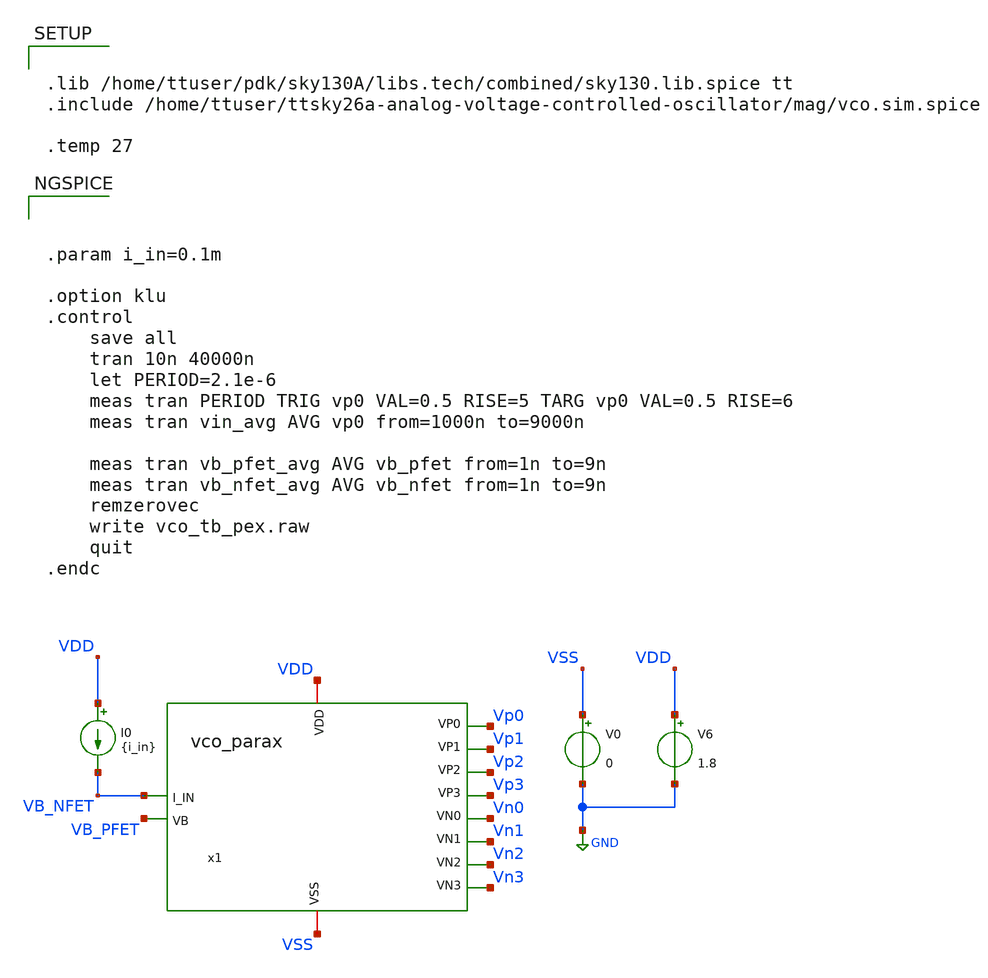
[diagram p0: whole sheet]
** sch_path: xschem/vco_tb_pex.sch
**.subckt vco_tb_pex
V0 VSS GND 0
V6 VDD GND 1.8
I0 VDD VB_NFET {i_in}
x1 VDD VSS VB_NFET Vp0 Vp1 Vp2 Vp3 Vn0 Vn1 Vn2 Vn3 VB_PFET vco_parax
**** begin user architecture code



.param i_in=0.1m

.option klu
.control
	save all
	tran 10n 40000n
	let PERIOD=2.1e-6
	meas tran PERIOD TRIG vp0 VAL=0.5 RISE=5 TARG vp0 VAL=0.5 RISE=6
	meas tran vin_avg AVG vp0 from=1000n to=9000n

	meas tran vb_pfet_avg AVG vb_pfet from=1n to=9n
	meas tran vb_nfet_avg AVG vb_nfet from=1n to=9n
	remzerovec
	write vco_tb_pex.raw
	quit
.endc




.lib /home/ttuser/pdk/sky130A/libs.tech/combined/sky130.lib.spice tt
.include /home/ttuser/ttsky26a-analog-voltage-controlled-oscillator/mag/vco.sim.spice

.temp 27


**** end user architecture code
**.ends

* expanding   symbol:  vco_parax.sym # of pins=12
** sym_path: xschem/vco.sym
.include [file normalize ../mag/vco.sim.spice]
.GLOBAL GND
.end
